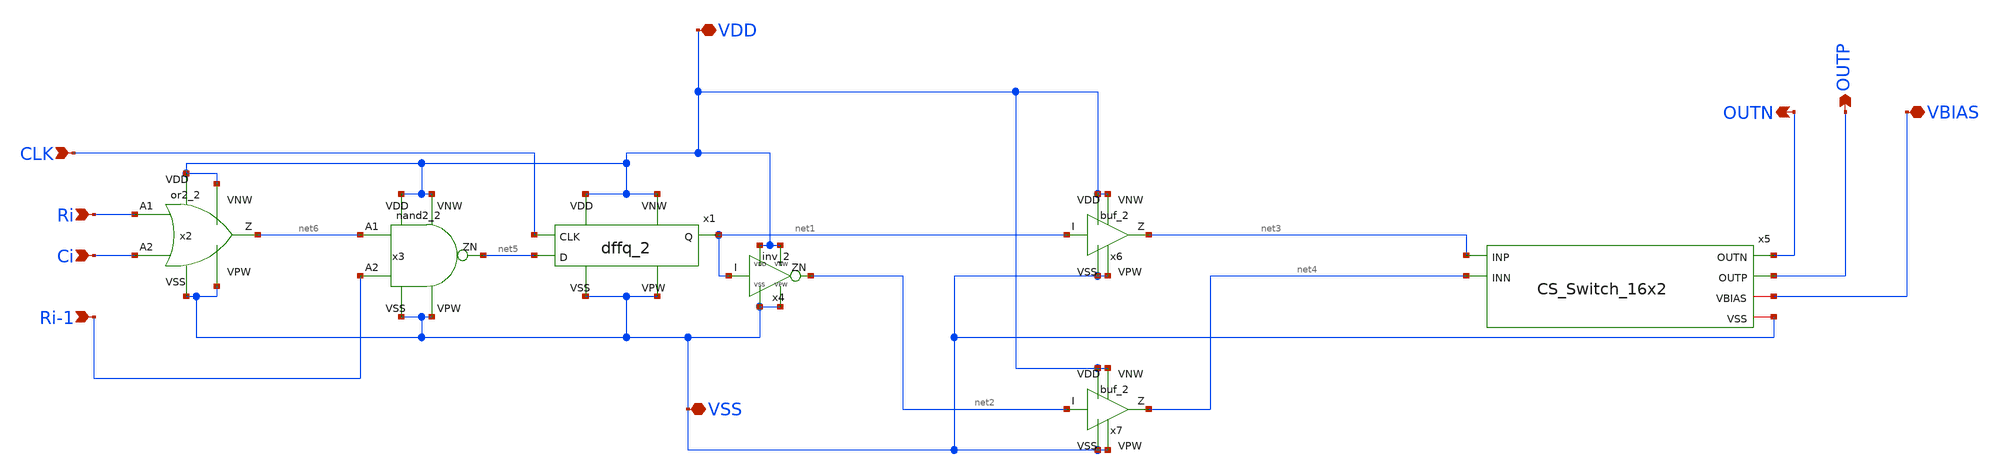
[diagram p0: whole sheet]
** sch_path: xschem/unit_cell_aray.sch
**.subckt unit_cell_aray Ri Ci Ri-1 CLK OUTP OUTN VBIAS VDD VSS
*.ipin Ri
*.ipin Ci
*.ipin Ri-1
*.ipin CLK
*.opin OUTP
*.opin OUTN
*.iopin VBIAS
*.iopin VDD
*.iopin VSS
x4 net1 net2 VDD VDD VSS VSS gf180mcu_fd_sc_mcu7t5v0__inv_2
x1 net5 CLK net1 VDD VDD VSS VSS gf180mcu_fd_sc_mcu7t5v0__dffq_2
x2 Ri Ci net6 VDD VDD VSS VSS gf180mcu_fd_sc_mcu7t5v0__or2_2
x3 net6 Ri-1 net5 VDD VDD VSS VSS gf180mcu_fd_sc_mcu7t5v0__nand2_2
x5 net3 net4 OUTP OUTN VBIAS VSS CS_Switch_16x2
x6 net1 net3 VDD VDD VSS VSS gf180mcu_fd_sc_mcu7t5v0__buf_2
x7 net2 net4 VDD VDD VSS VSS gf180mcu_fd_sc_mcu7t5v0__buf_2
**.ends
.end
